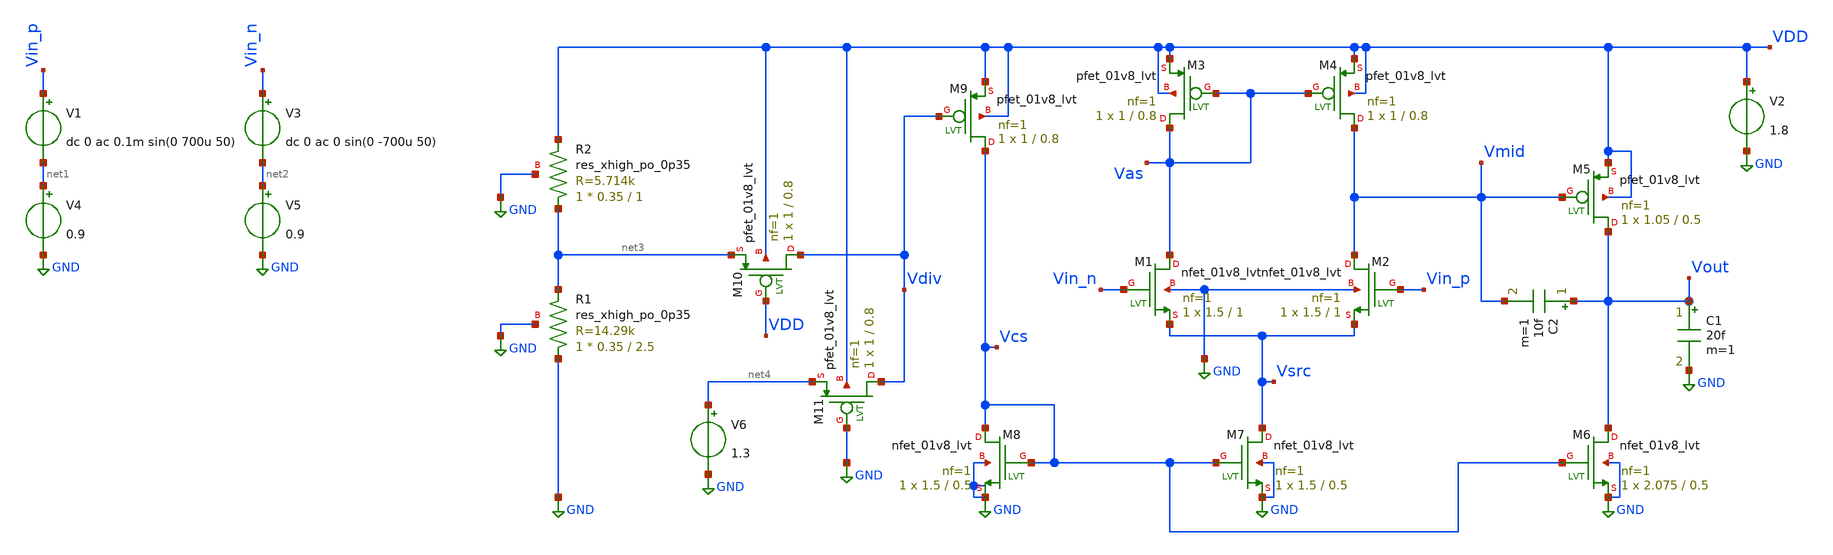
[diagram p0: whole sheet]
** sch_path: xchem/OTA2_lvt.sch
* Copyright 2021 Stefan Frederik Schippers
* Licensed under the Apache License, Version 2.0 (the "License");
* you may not use this file except in compliance with the License.
* You may obtain a copy of the License at
* https://www.apache.org/licenses/LICENSE-2.0
* Unless required by applicable law or agreed to in writing, software
* distributed under the License is distributed on an "AS IS" BASIS,
* WITHOUT WARRANTIES OR CONDITIONS OF ANY KIND, either express or implied.
* See the License for the specific language governing permissions and
* limitations under the License.
**.subckt OTA2_lvt
C1 Vout GND 20f m=1
V2 VDD GND 1.8
V1 Vin_p net1 dc 0 ac 0.1m sin(0 700u 50)
V3 Vin_n net2 dc 0 ac 0 sin(0 -700u 50)
V4 net1 GND 0.9
V5 net2 GND 0.9
XM1 Vas Vin_n Vsrc GND sky130_fd_pr__nfet_01v8_lvt L=1 W=1.5 nf=1 ad='int((nf+1)/2) * W/nf * 0.29' as='int((nf+2)/2) * W/nf * 0.29'
+ pd='2*int((nf+1)/2) * (W/nf + 0.29)' ps='2*int((nf+2)/2) * (W/nf + 0.29)' nrd='0.29 / W' nrs='0.29 / W'
+ sa=0 sb=0 sd=0 mult=1 m=1
XM2 Vmid Vin_p Vsrc GND sky130_fd_pr__nfet_01v8_lvt L=1 W=1.5 nf=1 ad='int((nf+1)/2) * W/nf * 0.29' as='int((nf+2)/2) * W/nf * 0.29'
+ pd='2*int((nf+1)/2) * (W/nf + 0.29)' ps='2*int((nf+2)/2) * (W/nf + 0.29)' nrd='0.29 / W' nrs='0.29 / W'
+ sa=0 sb=0 sd=0 mult=1 m=1
XM3 Vas Vas VDD VDD sky130_fd_pr__pfet_01v8_lvt L=0.8 W=1 nf=1 ad='int((nf+1)/2) * W/nf * 0.29' as='int((nf+2)/2) * W/nf * 0.29'
+ pd='2*int((nf+1)/2) * (W/nf + 0.29)' ps='2*int((nf+2)/2) * (W/nf + 0.29)' nrd='0.29 / W' nrs='0.29 / W'
+ sa=0 sb=0 sd=0 mult=1 m=1
XM4 Vmid Vas VDD VDD sky130_fd_pr__pfet_01v8_lvt L=0.8 W=1 nf=1 ad='int((nf+1)/2) * W/nf * 0.29' as='int((nf+2)/2) * W/nf * 0.29'
+ pd='2*int((nf+1)/2) * (W/nf + 0.29)' ps='2*int((nf+2)/2) * (W/nf + 0.29)' nrd='0.29 / W' nrs='0.29 / W'
+ sa=0 sb=0 sd=0 mult=1 m=1
XM5 Vout Vmid VDD VDD sky130_fd_pr__pfet_01v8_lvt L=0.5 W=1.05 nf=1 ad='int((nf+1)/2) * W/nf * 0.29'
+ as='int((nf+2)/2) * W/nf * 0.29' pd='2*int((nf+1)/2) * (W/nf + 0.29)' ps='2*int((nf+2)/2) * (W/nf + 0.29)'
+ nrd='0.29 / W' nrs='0.29 / W' sa=0 sb=0 sd=0 mult=1 m=1
XM6 Vout Vcs GND GND sky130_fd_pr__nfet_01v8_lvt L=0.5 W=2.075 nf=1 ad='int((nf+1)/2) * W/nf * 0.29'
+ as='int((nf+2)/2) * W/nf * 0.29' pd='2*int((nf+1)/2) * (W/nf + 0.29)' ps='2*int((nf+2)/2) * (W/nf + 0.29)'
+ nrd='0.29 / W' nrs='0.29 / W' sa=0 sb=0 sd=0 mult=1 m=1
XM7 Vsrc Vcs GND GND sky130_fd_pr__nfet_01v8_lvt L=0.5 W=1.5 nf=1 ad='int((nf+1)/2) * W/nf * 0.29' as='int((nf+2)/2) * W/nf * 0.29'
+ pd='2*int((nf+1)/2) * (W/nf + 0.29)' ps='2*int((nf+2)/2) * (W/nf + 0.29)' nrd='0.29 / W' nrs='0.29 / W'
+ sa=0 sb=0 sd=0 mult=1 m=1
XM8 Vcs Vcs GND GND sky130_fd_pr__nfet_01v8_lvt L=0.5 W=1.5 nf=1 ad='int((nf+1)/2) * W/nf * 0.29' as='int((nf+2)/2) * W/nf * 0.29'
+ pd='2*int((nf+1)/2) * (W/nf + 0.29)' ps='2*int((nf+2)/2) * (W/nf + 0.29)' nrd='0.29 / W' nrs='0.29 / W'
+ sa=0 sb=0 sd=0 mult=1 m=1
XR2 net3 VDD GND sky130_fd_pr__res_xhigh_po_0p35 L=1 mult=1 m=1
XR1 GND net3 GND sky130_fd_pr__res_xhigh_po_0p35 L=2.5 mult=1 m=1
XM9 Vcs Vdiv VDD VDD sky130_fd_pr__pfet_01v8_lvt L=0.8 W=1 nf=1 ad='int((nf+1)/2) * W/nf * 0.29' as='int((nf+2)/2) * W/nf * 0.29'
+ pd='2*int((nf+1)/2) * (W/nf + 0.29)' ps='2*int((nf+2)/2) * (W/nf + 0.29)' nrd='0.29 / W' nrs='0.29 / W'
+ sa=0 sb=0 sd=0 mult=1 m=1
C2 Vout Vmid 10f m=1
XM10 Vdiv VDD net3 VDD sky130_fd_pr__pfet_01v8_lvt L=0.8 W=1 nf=1 ad='int((nf+1)/2) * W/nf * 0.29' as='int((nf+2)/2) * W/nf * 0.29'
+ pd='2*int((nf+1)/2) * (W/nf + 0.29)' ps='2*int((nf+2)/2) * (W/nf + 0.29)' nrd='0.29 / W' nrs='0.29 / W'
+ sa=0 sb=0 sd=0 mult=1 m=1
XM11 Vdiv GND net4 VDD sky130_fd_pr__pfet_01v8_lvt L=0.8 W=1 nf=1 ad='int((nf+1)/2) * W/nf * 0.29' as='int((nf+2)/2) * W/nf * 0.29'
+ pd='2*int((nf+1)/2) * (W/nf + 0.29)' ps='2*int((nf+2)/2) * (W/nf + 0.29)' nrd='0.29 / W' nrs='0.29 / W'
+ sa=0 sb=0 sd=0 mult=1 m=1
V6 net4 GND 1.3
**** begin user architecture code


.control
run
save all
tran 10u 100m
plot Vout
*ac dec 101 1 1g
*plot db(1*V(Vout)/(V(Vin_p) - V(Vin_n))), 180/PI*phase(V(Vout))


let id1  = @m.xm1.msky130_fd_pr__nfet_01v8_lvt[id]
let id2  = @m.xm2.msky130_fd_pr__nfet_01v8_lvt[id]
let id3  = @m.xm3.msky130_fd_pr__pfet_01v8_lvt[id]
let id4  = @m.xm4.msky130_fd_pr__pfet_01v8_lvt[id]
let id5  = @m.xm5.msky130_fd_pr__pfet_01v8_lvt[id]
let id6  = @m.xm6.msky130_fd_pr__nfet_01v8_lvt[id]
let id7  = @m.xm7.msky130_fd_pr__nfet_01v8_lvt[id]
let id8  = @m.xm8.msky130_fd_pr__nfet_01v8_lvt[id]

let gm1  = @m.xm1.msky130_fd_pr__nfet_01v8_lvt[gm]
let gm2  = @m.xm2.msky130_fd_pr__nfet_01v8_lvt[gm]
let gm3  = @m.xm3.msky130_fd_pr__pfet_01v8_lvt[gm]
let gm4  = @m.xm4.msky130_fd_pr__pfet_01v8_lvt[gm]
let gm5  = @m.xm5.msky130_fd_pr__pfet_01v8_lvt[gm]
let gm6  = @m.xm6.msky130_fd_pr__nfet_01v8_lvt[gm]
let gm7  = @m.xm7.msky130_fd_pr__nfet_01v8_lvt[gm]
let gm8  = @m.xm8.msky130_fd_pr__nfet_01v8_lvt[gm]

let gds1  = @m.xm1.msky130_fd_pr__nfet_01v8_lvt[gds]
let gds2  = @m.xm2.msky130_fd_pr__nfet_01v8_lvt[gds]
let gds3  = @m.xm3.msky130_fd_pr__pfet_01v8_lvt[gds]
let gds4  = @m.xm4.msky130_fd_pr__pfet_01v8_lvt[gds]
let gds5  = @m.xm5.msky130_fd_pr__pfet_01v8_lvt[gds]
let gds6  = @m.xm6.msky130_fd_pr__nfet_01v8_lvt[gds]


print gm1/id1
print gm2/id2
print gm3/id3
print gm4/id4
print gm5/id5
print gm6/id6
print gm7/id7
print gm8/id8

.endc



** opencircuitdesign pdks install
.lib $::SKYWATER_MODELS/sky130.lib.spice tt


**** end user architecture code
**.ends
.GLOBAL GND
.end
